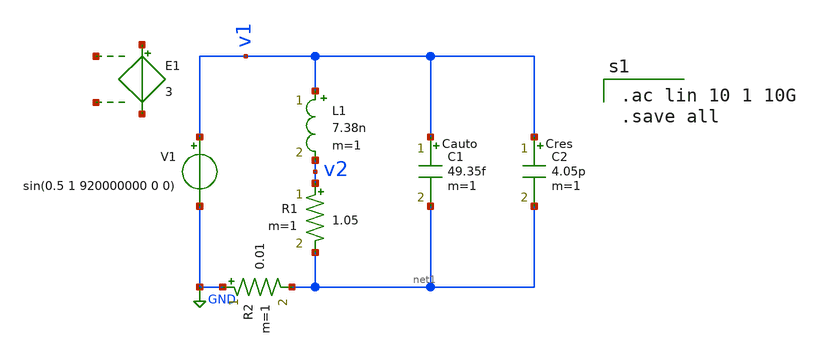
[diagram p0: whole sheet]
** sch_path: XSCHEM/RLC_tb.sch
**.subckt RLC_tb
C1 v1 net1 49.35f m=1
C2 v1 net1 4.05p m=1
L1 v1 v2 7.38n m=1
R1 v2 net1 1.05 m=1
V1 v1 GND sin(0.5 1 920000000 0 0)
R2 GND net1 0.01 m=1
E1 net2 net3 net4 net5 3
**** begin user architecture code

.ac lin 10 1 10G
.save all

**** end user architecture code
**.ends
.GLOBAL GND
.end
